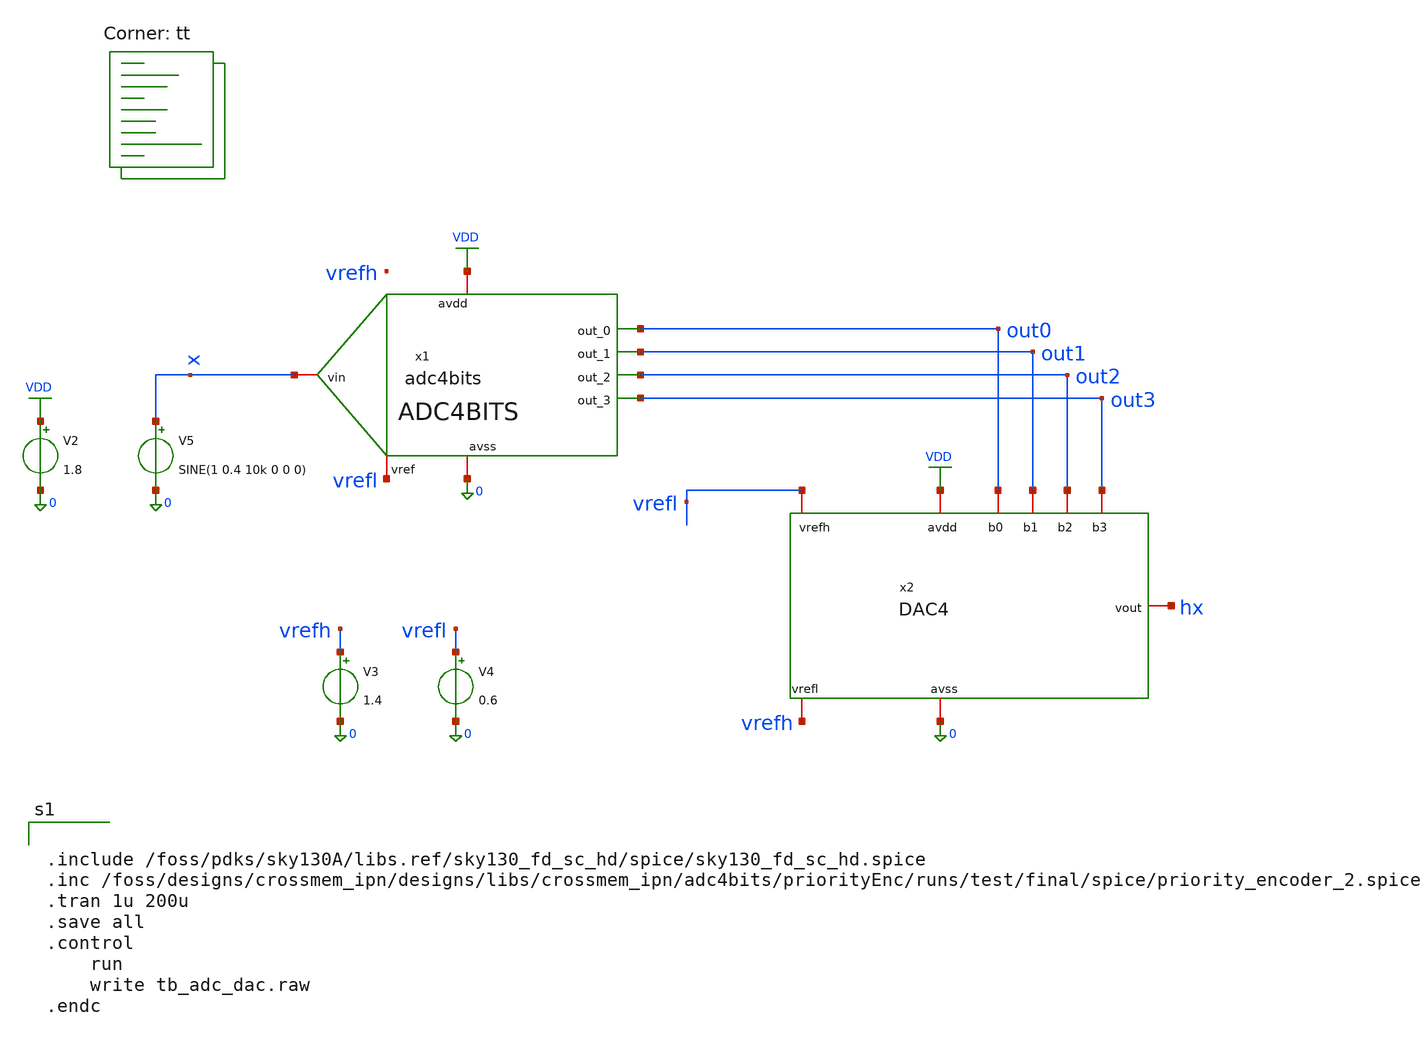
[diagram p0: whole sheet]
** sch_path: designs/libs/crossmem_ipn/tb_adc_dac.sch
**.subckt tb_adc_dac
x1 x vrefl out0 out1 out2 out3 0 VDD adc4bits
V2 VDD 0 1.8
x2 VDD out0 out1 0 out2 vrefl hx vrefh out3 DAC4
V3 vrefh 0 1.4
V4 vrefl 0 0.6
V5 x 0 SINE(1 0.4 10k 0 0 0)
**** begin user architecture code


.include /foss/pdks/sky130A/libs.ref/sky130_fd_sc_hd/spice/sky130_fd_sc_hd.spice
.inc /foss/designs/crossmem_ipn/designs/libs/crossmem_ipn/adc4bits/priorityEnc/runs/test/final/spice/priority_encoder_2.spice
.tran 1u 200u
.save all
.control
	run
	write tb_adc_dac.raw
.endc


.lib $::SKYWATER_MODELS/sky130.lib.spice tt
**** end user architecture code
**.ends
.GLOBAL VDD
.end
